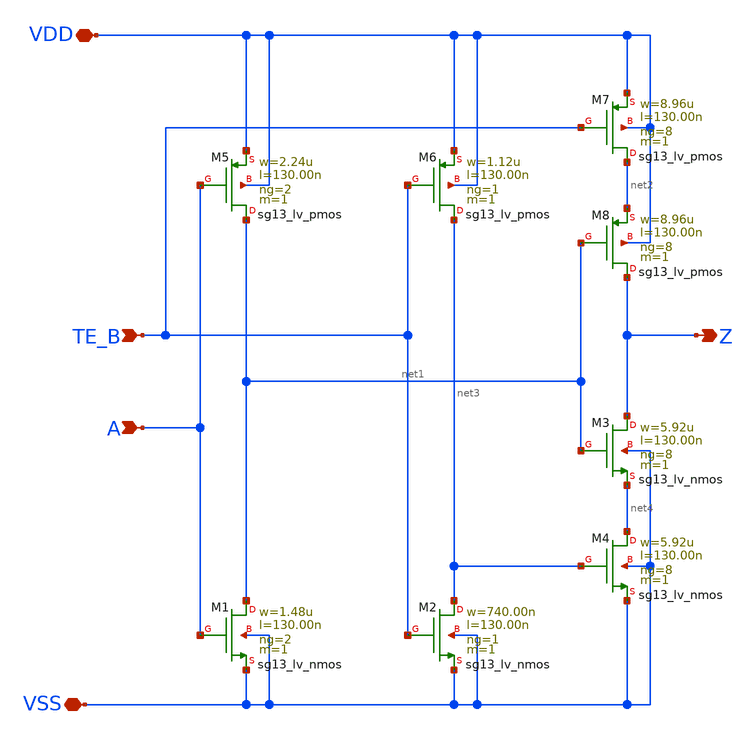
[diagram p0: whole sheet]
** sch_path: ihp-sg13g2/libs.tech/xschem/sg13g2_stdcells/sg13g2_ebufn_8.sch
* Copyright 2023 IHP PDK Authors
* Licensed under the Apache License, Version 2.0 (the "License");
* you may not use this file except in compliance with the License.
* You may obtain a copy of the License at
* https://www.apache.org/licenses/LICENSE-2.0
* Unless required by applicable law or agreed to in writing, software
* distributed under the License is distributed on an "AS IS" BASIS,
* WITHOUT WARRANTIES OR CONDITIONS OF ANY KIND, either express or implied.
* See the License for the specific language governing permissions and
* limitations under the License.
**.subckt sg13g2_ebufn_8 A TE_B Z VDD VSS
*.ipin A
*.ipin TE_B
*.opin Z
*.iopin VDD
*.iopin VSS
XM1 net1 A VSS VSS sg13_lv_nmos w=1.48u l=130.00n ng=2 m=1 mm_ok=1
XM2 net3 TE_B VSS VSS sg13_lv_nmos w=740.00n l=130.00n ng=1 m=1 mm_ok=1
XM3 Z net1 net4 VSS sg13_lv_nmos w=5.92u l=130.00n ng=8 m=1 mm_ok=1
XM4 net4 net3 VSS VSS sg13_lv_nmos w=5.92u l=130.00n ng=8 m=1 mm_ok=1
XM5 net1 A VDD VDD sg13_lv_pmos w=2.24u l=130.00n ng=2 m=1 mm_ok=1
XM6 net3 TE_B VDD VDD sg13_lv_pmos w=1.12u l=130.00n ng=1 m=1 mm_ok=1
XM7 net2 TE_B VDD VDD sg13_lv_pmos w=8.96u l=130.00n ng=8 m=1 mm_ok=1
XM8 Z net1 net2 VDD sg13_lv_pmos w=8.96u l=130.00n ng=8 m=1 mm_ok=1
**.ends
.end
